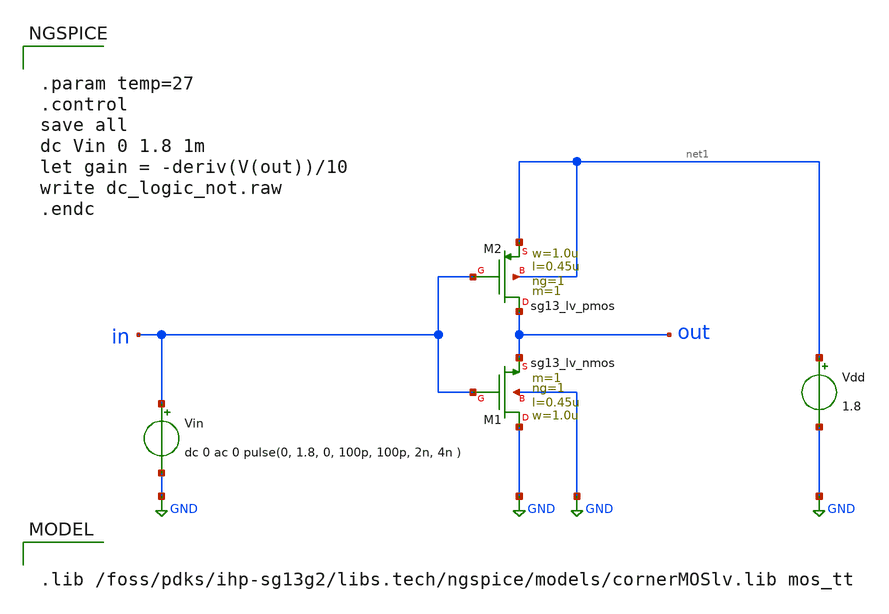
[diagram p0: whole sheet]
** sch_path: content/simulation_files/xschem/05_dc_logic_not.sch
* Copyright 2023 IHP PDK Authors
**.subckt 05_dc_logic_not
Vin in GND dc 0 ac 0 pulse(0, 1.8, 0, 100p, 100p, 2n, 4n )
Vdd net1 GND 1.8
XM1 GND in out GND sg13_lv_nmos w=1.0u l=0.45u ng=1 m=1 mm_ok=1
XM2 out in net1 net1 sg13_lv_pmos w=1.0u l=0.45u ng=1 m=1 mm_ok=1
**** begin user architecture code

.lib /foss/pdks/ihp-sg13g2/libs.tech/ngspice/models/cornerMOSlv.lib mos_tt



.param temp=27
.control
save all
dc Vin 0 1.8 1m
let gain = -deriv(V(out))/10
write dc_logic_not.raw
.endc


**** end user architecture code
**.ends
.GLOBAL GND
.end
